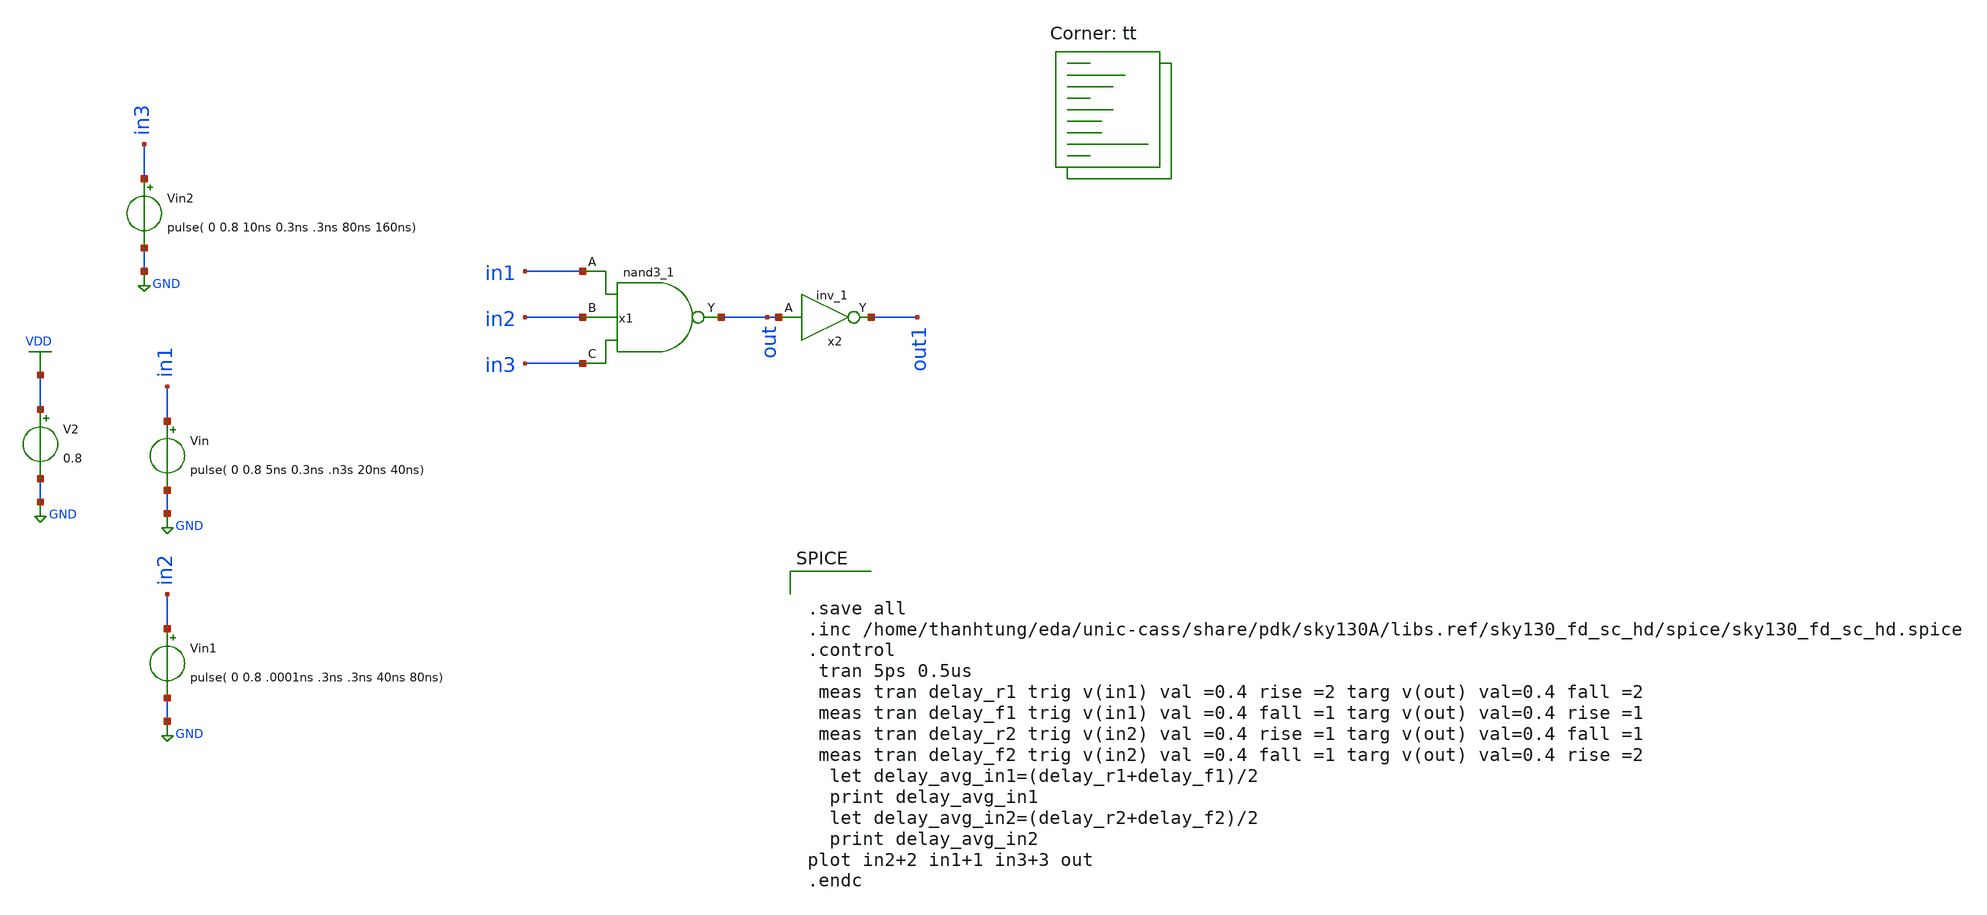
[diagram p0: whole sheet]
** sch_path: nand3_para.sch
**.subckt nand3_para
V2 VDD GND 0.8
Vin in1 GND pulse( 0 0.8 5ns 0.3ns .n3s 20ns 40ns)
x1 in1 in2 in3 GND GND VDD VDD out sky130_fd_sc_hd__nand3_1
Vin1 in2 GND pulse( 0 0.8 .0001ns .3ns .3ns 40ns 80ns)
Vin2 in3 GND pulse( 0 0.8 10ns 0.3ns .3ns 80ns 160ns)
x2 out GND GND VDD VDD out1 sky130_fd_sc_hd__inv_1
**** begin user architecture code


.save all
.inc /home/thanhtung/eda/unic-cass/share/pdk/sky130A/libs.ref/sky130_fd_sc_hd/spice/sky130_fd_sc_hd.spice
.control
 tran 5ps 0.5us
 meas tran delay_r1 trig v(in1) val =0.4 rise =2 targ v(out) val=0.4 fall =2
 meas tran delay_f1 trig v(in1) val =0.4 fall =1 targ v(out) val=0.4 rise =1
 meas tran delay_r2 trig v(in2) val =0.4 rise =1 targ v(out) val=0.4 fall =1
 meas tran delay_f2 trig v(in2) val =0.4 fall =1 targ v(out) val=0.4 rise =2
  let delay_avg_in1=(delay_r1+delay_f1)/2
  print delay_avg_in1
  let delay_avg_in2=(delay_r2+delay_f2)/2
  print delay_avg_in2
plot in2+2 in1+1 in3+3 out
.endc


.lib $::SKYWATER_MODELS/sky130.lib.spice tt
**** end user architecture code
**.ends
.GLOBAL GND
.GLOBAL VDD
.end
